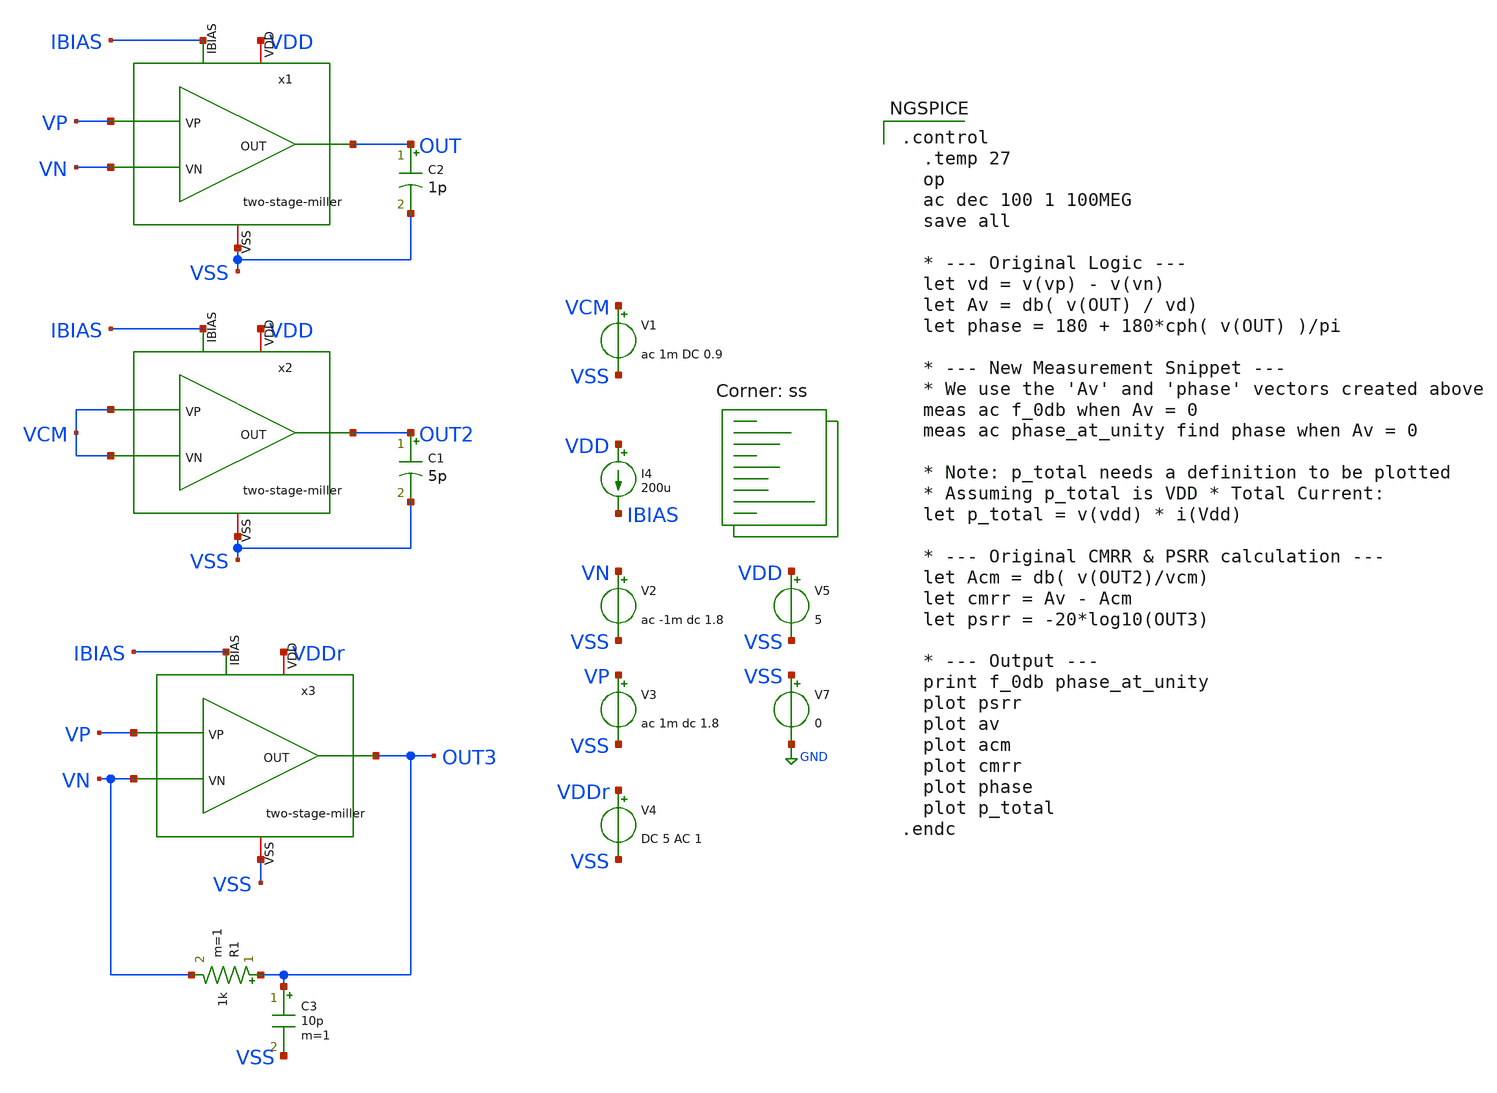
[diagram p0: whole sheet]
** sch_path: xschem/error-amplifier/testbench/tb_ac.sch
**.subckt tb_ac
V2 VN VSS ac -1m dc 1.8
V3 VP VSS ac 1m dc 1.8
V5 VDD VSS 5
V7 VSS GND 0
C2 OUT VSS 1p m=1
I4 VDD IBIAS 200u
C1 OUT2 VSS 5p m=1
V1 VCM VSS ac 1m DC 0.9
C3 OUT3 VSS 10p m=1
R1 OUT3 VN 1k m=1
V4 VDDr VSS DC 5 AC 1
x1 VDD OUT VP VN IBIAS VSS two-stage-miller
x2 VDD OUT2 VCM VCM IBIAS VSS two-stage-miller
x3 VDDr OUT3 VP VN IBIAS VSS two-stage-miller
**** begin user architecture code

.control
  .temp 27
  op
  ac dec 100 1 100MEG
  save all

  * --- Original Logic ---
  let vd = v(vp) - v(vn)
  let Av = db( v(OUT) / vd)
  let phase = 180 + 180*cph( v(OUT) )/pi

  * --- New Measurement Snippet ---
  * We use the 'Av' and 'phase' vectors created above
  meas ac f_0db when Av = 0
  meas ac phase_at_unity find phase when Av = 0

  * Note: p_total needs a definition to be plotted
  * Assuming p_total is VDD * Total Current:
  let p_total = v(vdd) * i(Vdd)

  * --- Original CMRR & PSRR calculation ---
  let Acm = db( v(OUT2)/vcm)
  let cmrr = Av - Acm
  let psrr = -20*log10(OUT3)

  * --- Output ---
  print f_0db phase_at_unity
  plot psrr
  plot av
  plot acm
  plot cmrr
  plot phase
  plot p_total
.endc



.lib $::SKYWATER_MODELS/sky130.lib.spice ss
**** end user architecture code
**.ends

* expanding   symbol:  icdec-biomedical-pmic/xschem/error-amplifier/schematics/two-stage-miller.sym
*+ # of pins=6
** sym_path: xschem/error-amplifier/schematics/two-stage-miller.sym
** sch_path: xschem/error-amplifier/schematics/two-stage-miller.sch
.subckt two-stage-miller VDD OUT VP VN IBIAS VSS
*.iopin VDD
*.iopin VSS
*.ipin IBIAS
*.ipin VP
*.ipin VN
*.opin OUT
XM1 net3 net2 VDD VDD sky130_fd_pr__pfet_g5v0d10v5 L=1.25 W=75.2 nf=8 ad='int((nf+1)/2) * W/nf * 0.29'
+ as='int((nf+2)/2) * W/nf * 0.29' pd='2*int((nf+1)/2) * (W/nf + 0.29)' ps='2*int((nf+2)/2) * (W/nf + 0.29)'
+ nrd='0.29 / W' nrs='0.29 / W' sa=0 sb=0 sd=0 mult=1 m=1
XM2 net2 net2 VDD VDD sky130_fd_pr__pfet_g5v0d10v5 L=1.25 W=75.2 nf=8 ad='int((nf+1)/2) * W/nf * 0.29'
+ as='int((nf+2)/2) * W/nf * 0.29' pd='2*int((nf+1)/2) * (W/nf + 0.29)' ps='2*int((nf+2)/2) * (W/nf + 0.29)'
+ nrd='0.29 / W' nrs='0.29 / W' sa=0 sb=0 sd=0 mult=1 m=1
XM3 net3 VN net1 VSS sky130_fd_pr__nfet_g5v0d10v5 L=0.5 W=37.7 nf=8 ad='int((nf+1)/2) * W/nf * 0.29'
+ as='int((nf+2)/2) * W/nf * 0.29' pd='2*int((nf+1)/2) * (W/nf + 0.29)' ps='2*int((nf+2)/2) * (W/nf + 0.29)'
+ nrd='0.29 / W' nrs='0.29 / W' sa=0 sb=0 sd=0 mult=1 m=1
XM4 net2 VP net1 VSS sky130_fd_pr__nfet_g5v0d10v5 L=0.5 W=37.7 nf=8 ad='int((nf+1)/2) * W/nf * 0.29'
+ as='int((nf+2)/2) * W/nf * 0.29' pd='2*int((nf+1)/2) * (W/nf + 0.29)' ps='2*int((nf+2)/2) * (W/nf + 0.29)'
+ nrd='0.29 / W' nrs='0.29 / W' sa=0 sb=0 sd=0 mult=1 m=1
XM5 net1 IBIAS VSS VSS sky130_fd_pr__nfet_g5v0d10v5 L=1.25 W=60 nf=8 ad='int((nf+1)/2) * W/nf * 0.29'
+ as='int((nf+2)/2) * W/nf * 0.29' pd='2*int((nf+1)/2) * (W/nf + 0.29)' ps='2*int((nf+2)/2) * (W/nf + 0.29)'
+ nrd='0.29 / W' nrs='0.29 / W' sa=0 sb=0 sd=0 mult=1 m=1
XM6 IBIAS IBIAS VSS VSS sky130_fd_pr__nfet_g5v0d10v5 L=1.25 W=60 nf=8 ad='int((nf+1)/2) * W/nf * 0.29'
+ as='int((nf+2)/2) * W/nf * 0.29' pd='2*int((nf+1)/2) * (W/nf + 0.29)' ps='2*int((nf+2)/2) * (W/nf + 0.29)'
+ nrd='0.29 / W' nrs='0.29 / W' sa=0 sb=0 sd=0 mult=1 m=1
XM7 OUT net3 VDD VDD sky130_fd_pr__pfet_g5v0d10v5 L=1.25 W=160 nf=16 ad='int((nf+1)/2) * W/nf * 0.29'
+ as='int((nf+2)/2) * W/nf * 0.29' pd='2*int((nf+1)/2) * (W/nf + 0.29)' ps='2*int((nf+2)/2) * (W/nf + 0.29)'
+ nrd='0.29 / W' nrs='0.29 / W' sa=0 sb=0 sd=0 mult=1 m=1
XM8 OUT IBIAS VSS VSS sky130_fd_pr__nfet_g5v0d10v5 L=1.25 W=60 nf=8 ad='int((nf+1)/2) * W/nf * 0.29'
+ as='int((nf+2)/2) * W/nf * 0.29' pd='2*int((nf+1)/2) * (W/nf + 0.29)' ps='2*int((nf+2)/2) * (W/nf + 0.29)'
+ nrd='0.29 / W' nrs='0.29 / W' sa=0 sb=0 sd=0 mult=1 m=1
XC1 net4 net3 sky130_fd_pr__cap_mim_m3_1 W=25 L=25 MF=8 m=8
XM9 OUT VSS net4 net4 sky130_fd_pr__pfet_g5v0d10v5 L=0.9 W=20 nf=4 ad='int((nf+1)/2) * W/nf * 0.29' as='int((nf+2)/2) * W/nf * 0.29'
+ pd='2*int((nf+1)/2) * (W/nf + 0.29)' ps='2*int((nf+2)/2) * (W/nf + 0.29)' nrd='0.29 / W' nrs='0.29 / W'
+ sa=0 sb=0 sd=0 mult=1 m=1
.ends

.GLOBAL GND
.end
